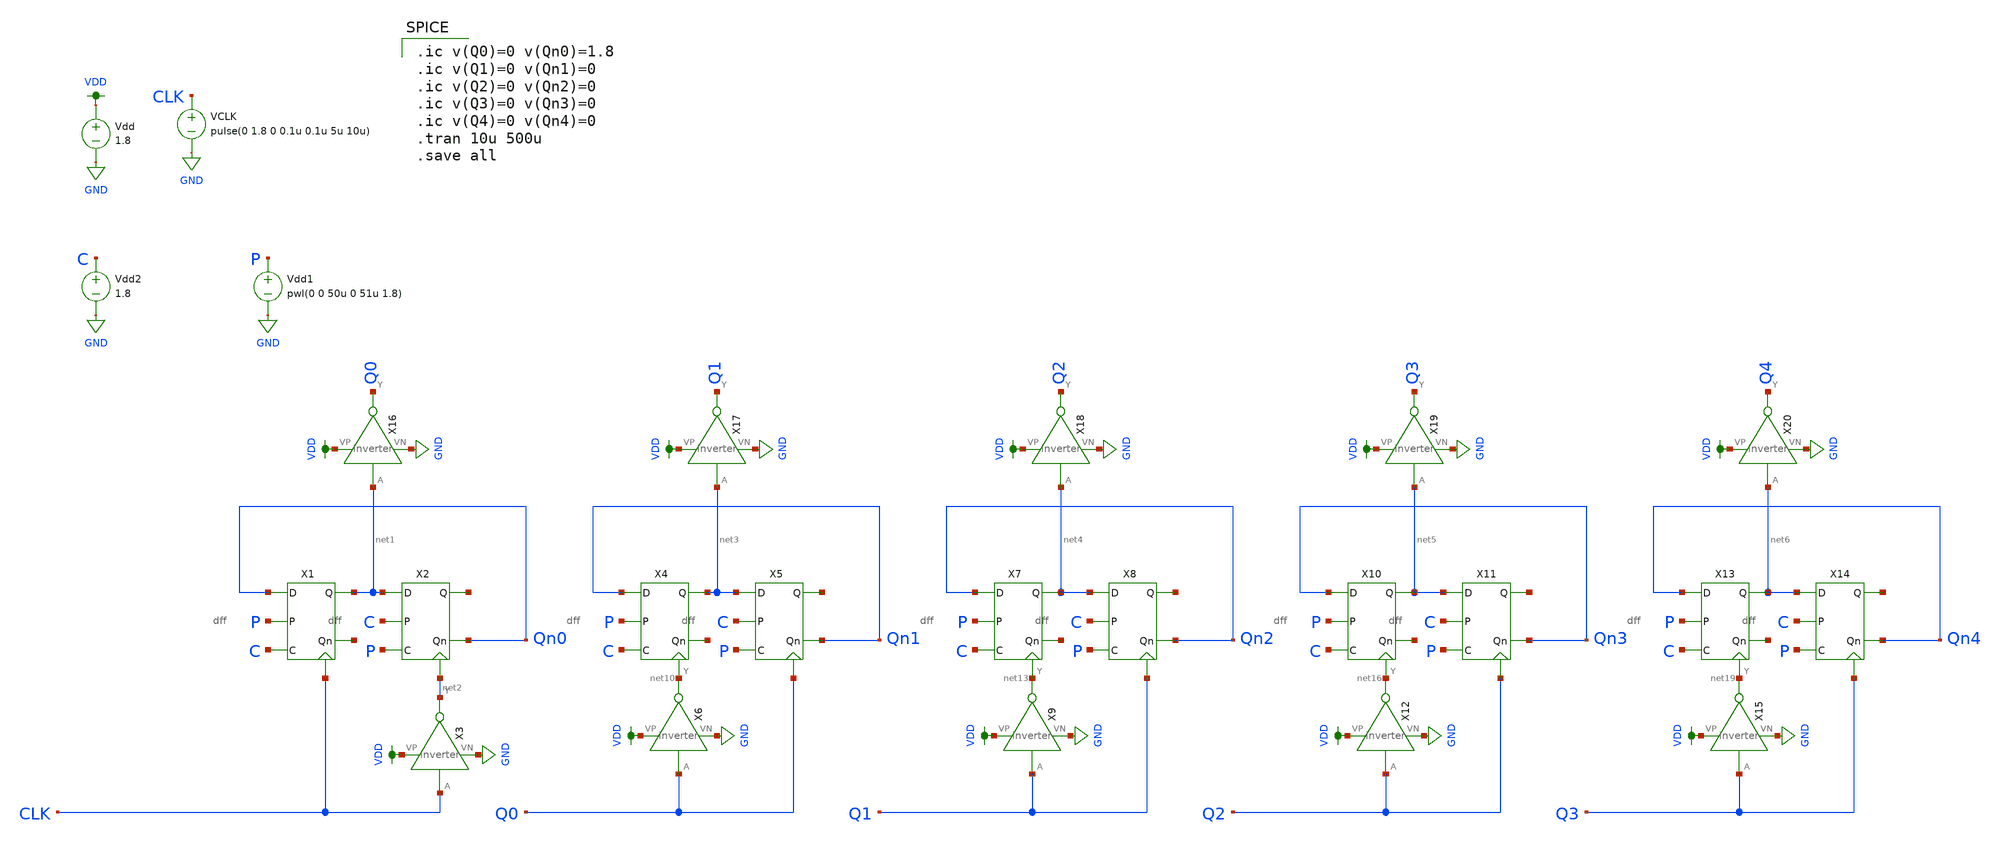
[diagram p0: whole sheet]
** sch_path: schematic/counter_new.sch
**.subckt counter_new
Vdd VDD GND 1.8
VCLK CLK GND pulse(0 1.8 0 0.1u 0.1u 5u 10u)
X1 Qn0 net7 net1 CLK P C dff
X2 net1 Qn0 net8 net2 C P dff
X3 CLK net2 VDD GND inverter
X4 Qn1 net9 net3 net10 P C dff
X5 net3 Qn1 net11 Q0 C P dff
X6 Q0 net10 VDD GND inverter
X7 Qn2 net12 net4 net13 P C dff
X8 net4 Qn2 net14 Q1 C P dff
X10 Qn3 net15 net5 net16 P C dff
X11 net5 Qn3 net17 Q2 C P dff
X13 Qn4 net18 net6 net19 P C dff
X14 net6 Qn4 net20 Q3 C P dff
X9 Q1 net13 VDD GND inverter
X12 Q2 net16 VDD GND inverter
X15 Q3 net19 VDD GND inverter
X16 net1 Q0 VDD GND inverter
X17 net3 Q1 VDD GND inverter
X18 net4 Q2 VDD GND inverter
X19 net5 Q3 VDD GND inverter
X20 net6 Q4 VDD GND inverter
Vdd1 P GND pwl(0 0 50u 0 51u 1.8)
Vdd2 C GND 1.8
**** begin user architecture code

.ic v(Q0)=0 v(Qn0)=1.8
.ic v(Q1)=0 v(Qn1)=0
.ic v(Q2)=0 v(Qn2)=0
.ic v(Q3)=0 v(Qn3)=0
.ic v(Q4)=0 v(Qn4)=0
.tran 10u 500u
.save all


.option wnflag=1
.param MC_SWITCH=0.0
.lib ~/skywater/skywater-pdk/libraries/sky130_fd_pr_ngspice/latest/models/sky130.lib.spice tt

**** end user architecture code
**.ends
.GLOBAL GND
.GLOBAL VDD
.end
